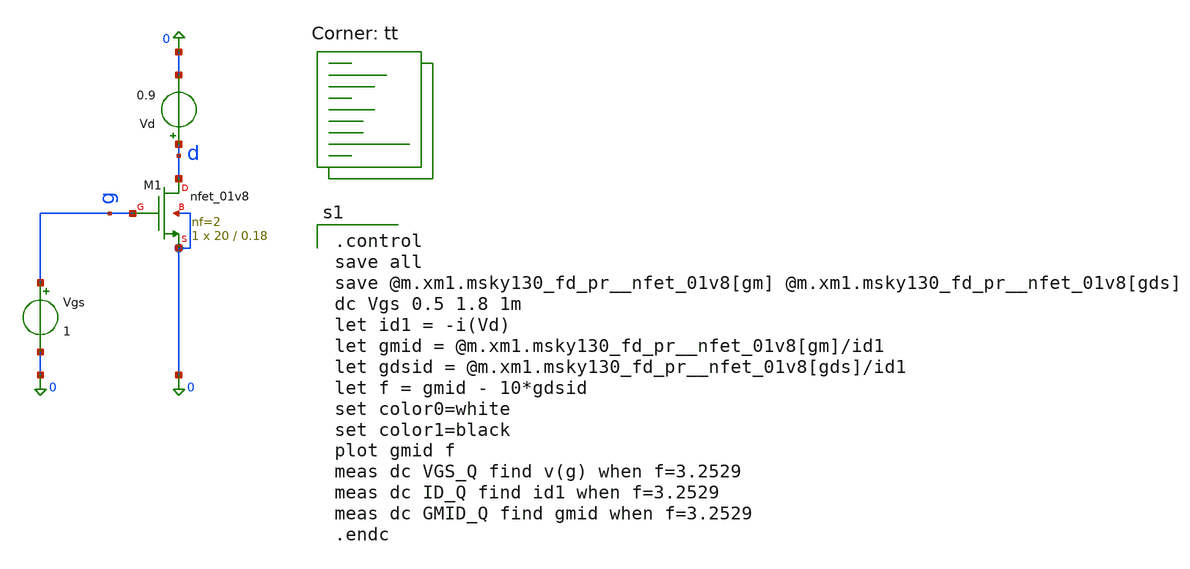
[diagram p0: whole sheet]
** sch_path: Homework 4 - Differential Pair Small Signal Gain/Simulations/ex5_nmos.sch
**.subckt ex5_nmos
Vgs g 0 1
XM1 d g 0 0 sky130_fd_pr__nfet_01v8 L=0.18 W=20 nf=2 ad='int((2 + 1)/2) * 20 / 2 * 0.29' as='int((2 + 2)/2) * 20 / 2 * 0.29'
+ pd='2*int((2 + 1)/2) * (20 / 2 + 0.29)' ps='2*int((2 + 2)/2) * (20 / 2 + 0.29)' nrd='0.29 / 20 ' nrs='0.29 / 20 '
+ sa=0 sb=0 sd=0 mult=1 m=1
Vd d 0 0.9
**** begin user architecture code
.lib $::SKYWATER_MODELS/sky130.lib.spice tt

.control
save all
save @m.xm1.msky130_fd_pr__nfet_01v8[gm] @m.xm1.msky130_fd_pr__nfet_01v8[gds]
dc Vgs 0.5 1.8 1m
let id1 = -i(Vd)
let gmid = @m.xm1.msky130_fd_pr__nfet_01v8[gm]/id1
let gdsid = @m.xm1.msky130_fd_pr__nfet_01v8[gds]/id1
let f = gmid - 10*gdsid
set color0=white
set color1=black
plot gmid f
meas dc VGS_Q find v(g) when f=3.2529
meas dc ID_Q find id1 when f=3.2529
meas dc GMID_Q find gmid when f=3.2529
.endc



**** end user architecture code
**.ends
.end
